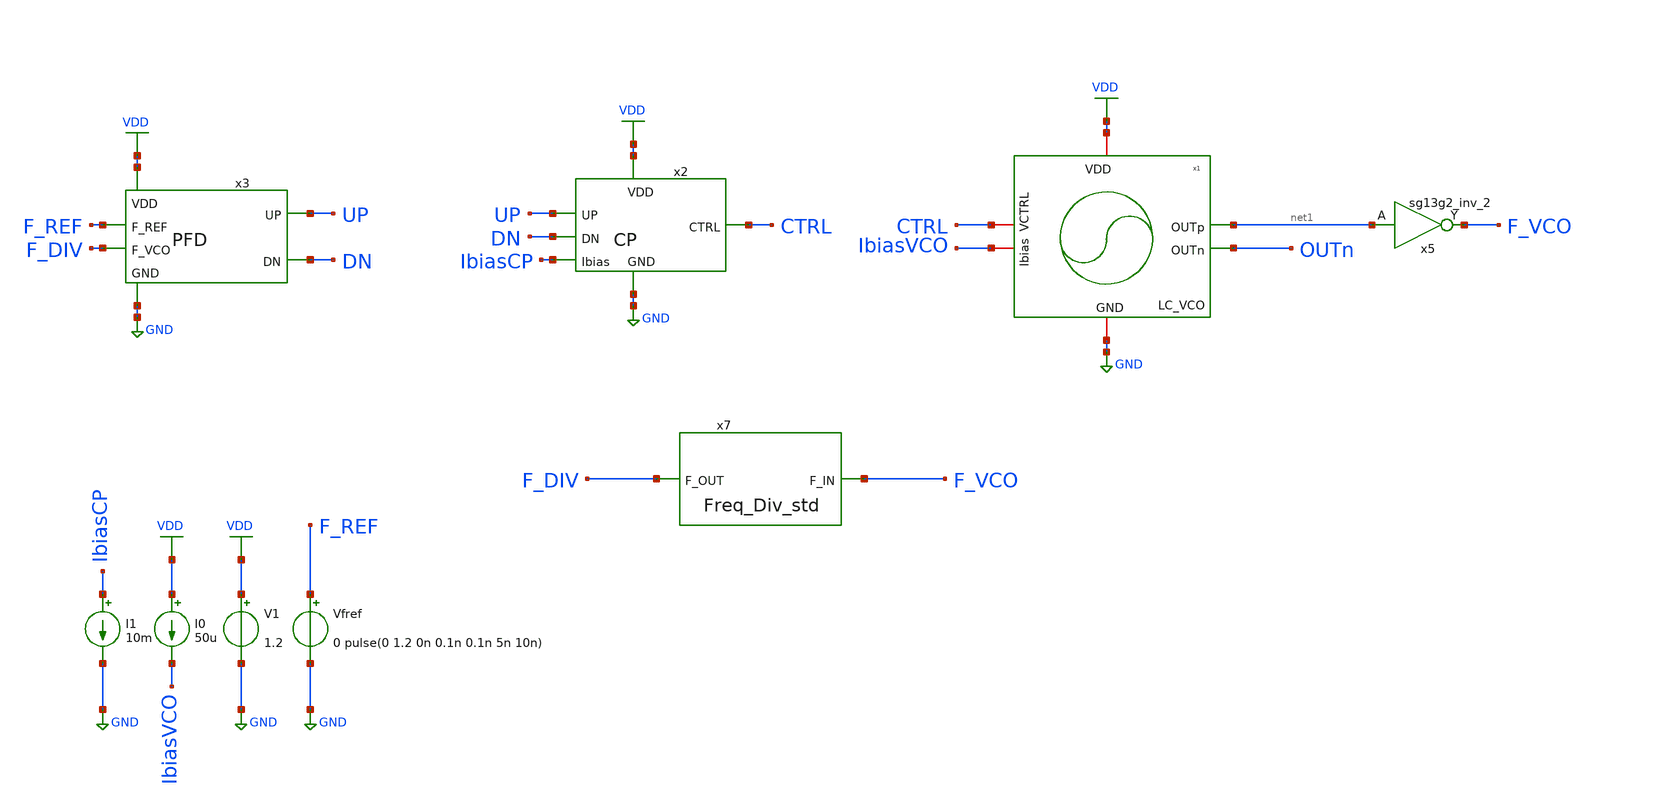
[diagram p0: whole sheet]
** sch_path: xschem/Test/pll_temp_fredivider_tb.sch
**.subckt pll_temp_fredivider_tb
V1 VDD GND 1.2
I0 VDD IbiasVCO 50u
Vfref F_REF GND 0 pulse(0 1.2 0n 0.1n 0.1n 5n 10n)
I1 IbiasCP GND 10m
x5 F_VCO net1 VDD GND sg13g2_inv_2
x2 VDD UP CTRL DN GND IbiasCP CP
x3 VDD UP F_REF F_DIV DN GND PFD
x4 VDD net1 OUTn IbiasVCO CTRL GND LC_VCO
x7 F_VCO F_DIV Freq_Div_std
**** begin user architecture code



.lib cornerMOSlv.lib mos_tt
.lib cornerHBT.lib hbt_typ
.lib cornerRES.lib res_typ
.lib cornerCAP.lib cap_typ_stat
.include /foss/pdks/ihp-sg13g2/libs.ref/sg13g2_stdcell/spice/sg13g2_stdcell.spice
.global VDD GND


.param CP_N_L = 0.5u
.param CP_N_W = 10u
.param CP_P_M = 1
.param CP_P_L = 0.5u
.param CP_P_W = 30u
.param CP_N_M = 1
.param C_CP = 400p






.model freq_div freq_div
.include ./IHP_4nH_Inductor.spice
.option temp = 27
.param VDD = 1.2
.ic v(OUTp)=0.6

.control
.options maxstep=100P reltol=1e-3 abstol=1e-6
pre_osdi ./freq_div.osdi
save v(CTRL) v(OUTp) v(F_REF) v(F_DIV) v(VDD) v(UP) v(DN) v(F_VCO)

tran 50p 500n uic
write tb_pll_freq_div.raw
*quit 0
.endc



**** end user architecture code
**.ends
.GLOBAL GND
.GLOBAL VDD
.end
